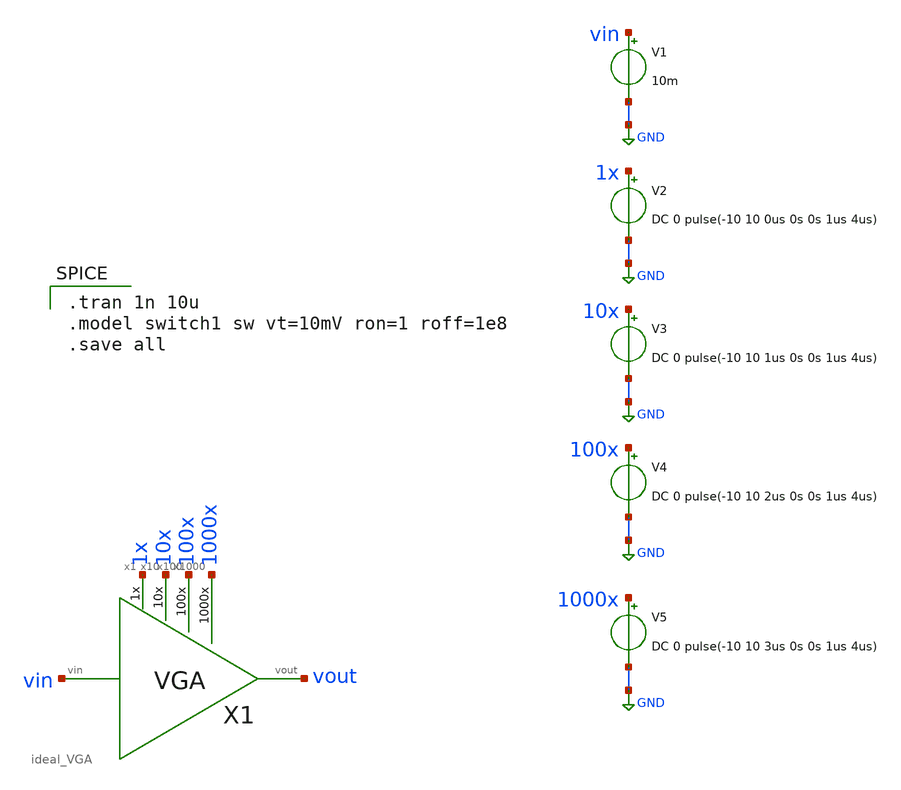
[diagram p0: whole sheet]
** sch_path: xschem/VGA/ideal_VGA_TB.sch
**.subckt ideal_VGA_TB
X1 vin vout 1x 10x 100x 1000x ideal_VGA
V1 vin GND 10m
V2 1x GND DC 0 pulse(-10 10 0us 0s 0s 1us 4us)
V3 10x GND DC 0 pulse(-10 10 1us 0s 0s 1us 4us)
V4 100x GND DC 0 pulse(-10 10 2us 0s 0s 1us 4us)
V5 1000x GND DC 0 pulse(-10 10 3us 0s 0s 1us 4us)
**** begin user architecture code

.tran 1n 10u
.model switch1 sw vt=10mV ron=1 roff=1e8
.save all

**** end user architecture code
**.ends

* expanding   symbol:  ideal_VGA.sym # of pins=6
** sym_path: xschem/VGA/ideal_VGA.sym
** sch_path: xschem/VGA/ideal_VGA.sch
.subckt ideal_VGA vin vout x1 x10 x100 x1000
*.ipin vin
*.ipin x1
*.ipin x10
*.ipin x100
*.ipin x1000
*.opin vout
X1 vin net1 vout opamp
R1 net1 GND 1k m=1
R2 net2 net1 9k m=1
R3 net3 net1 99k m=1
R4 net4 net1 999k m=1
S5 vout net1 x1 GND switch1 OFF
S1 vout net2 x10 GND switch1 OFF
S2 vout net3 x100 GND switch1 OFF
S3 vout net4 x1000 GND switch1 OFF
.ends


* expanding   symbol:  MISC/opamp.sym # of pins=3
** sym_path: xschem/MISC/opamp.sym
** sch_path: xschem/MISC/opamp.sch
.subckt opamp vp vm out
*.ipin vp
*.ipin vm
*.opin out
E1 out GND vp vm 1E6
.ends

.GLOBAL GND
.end
